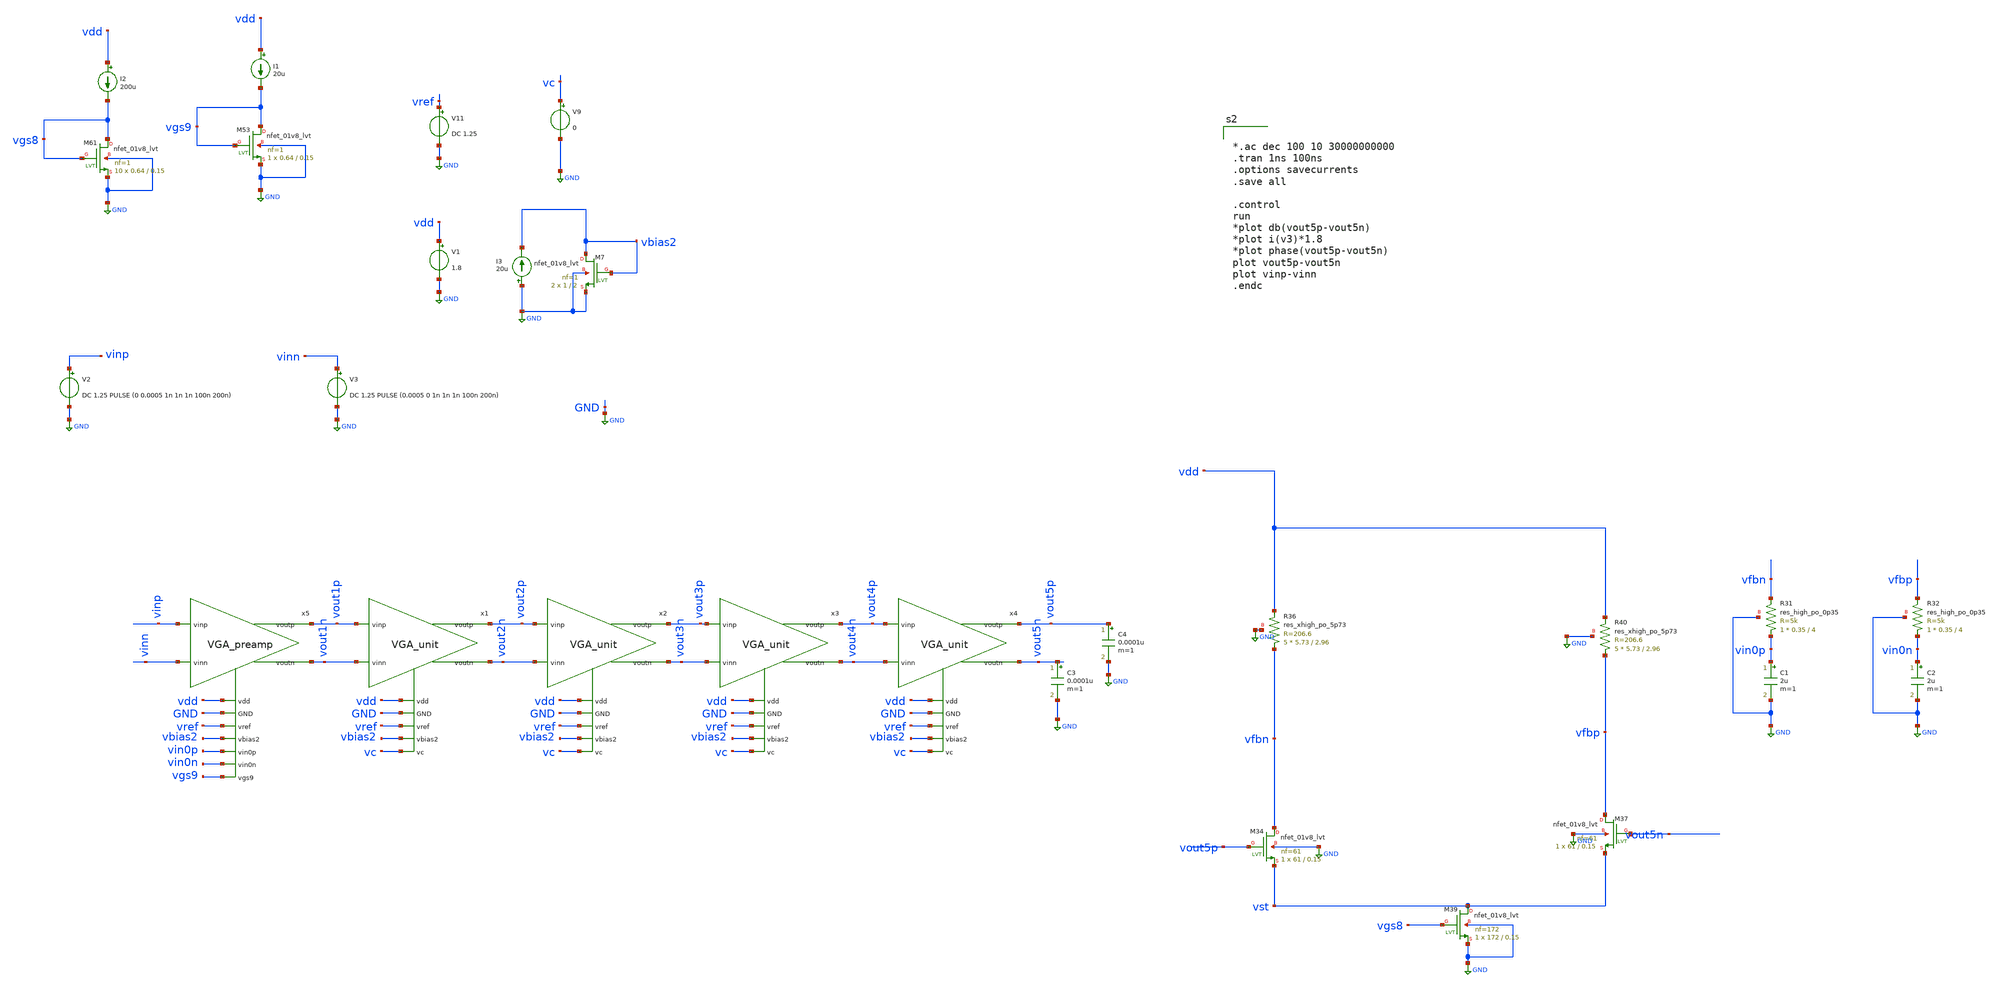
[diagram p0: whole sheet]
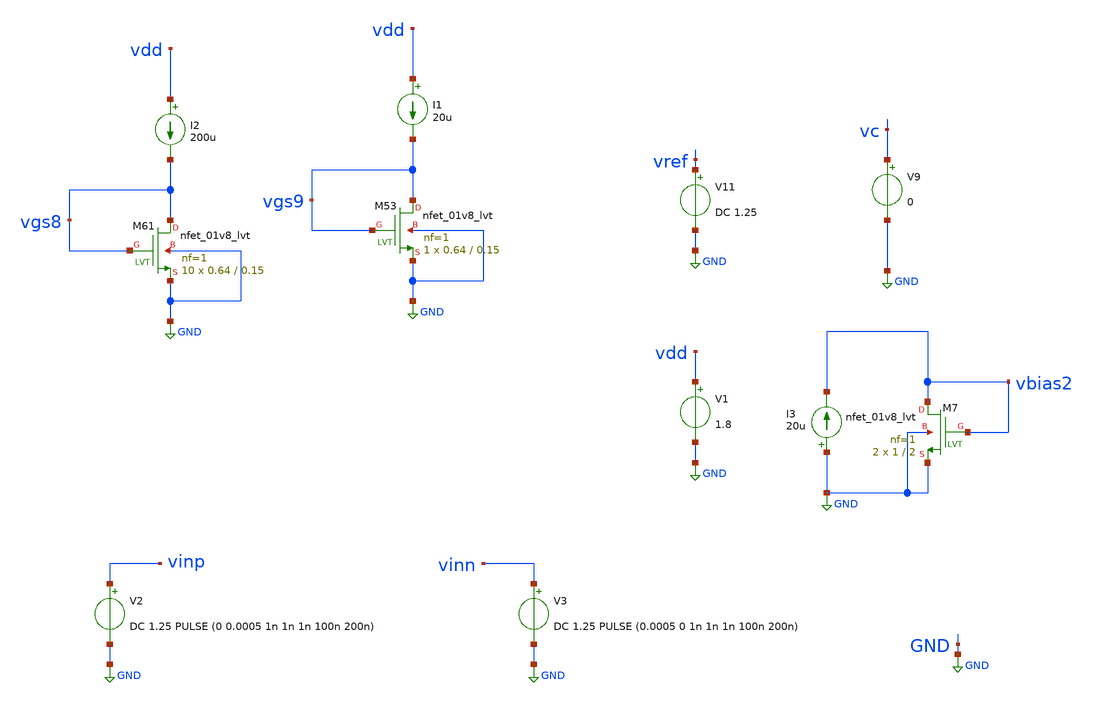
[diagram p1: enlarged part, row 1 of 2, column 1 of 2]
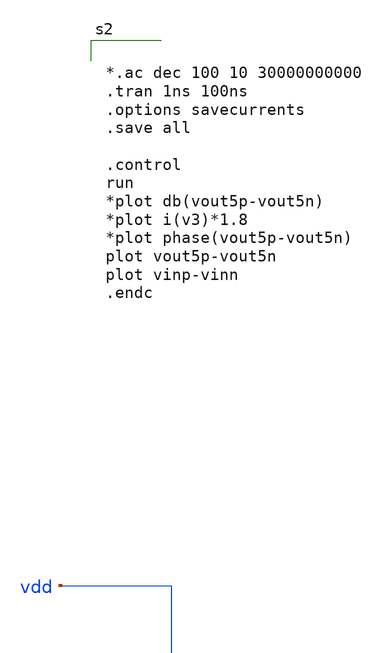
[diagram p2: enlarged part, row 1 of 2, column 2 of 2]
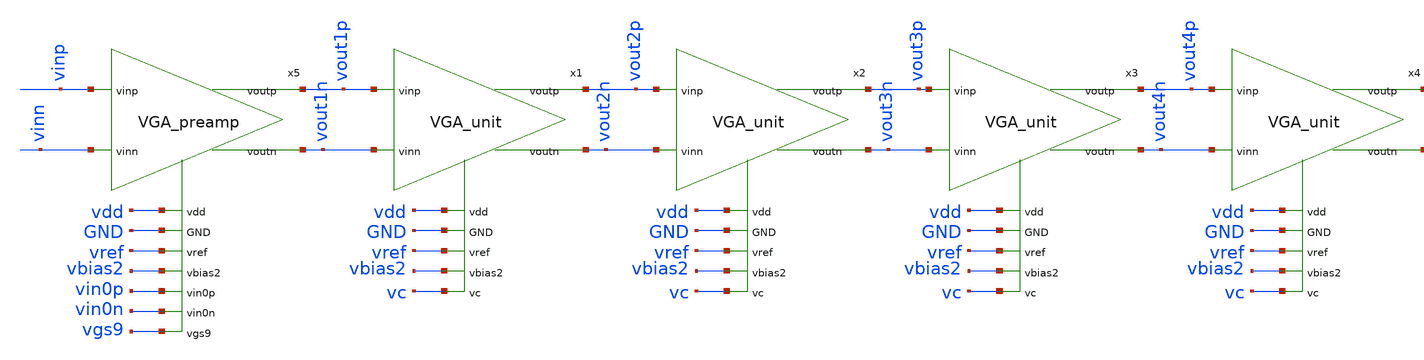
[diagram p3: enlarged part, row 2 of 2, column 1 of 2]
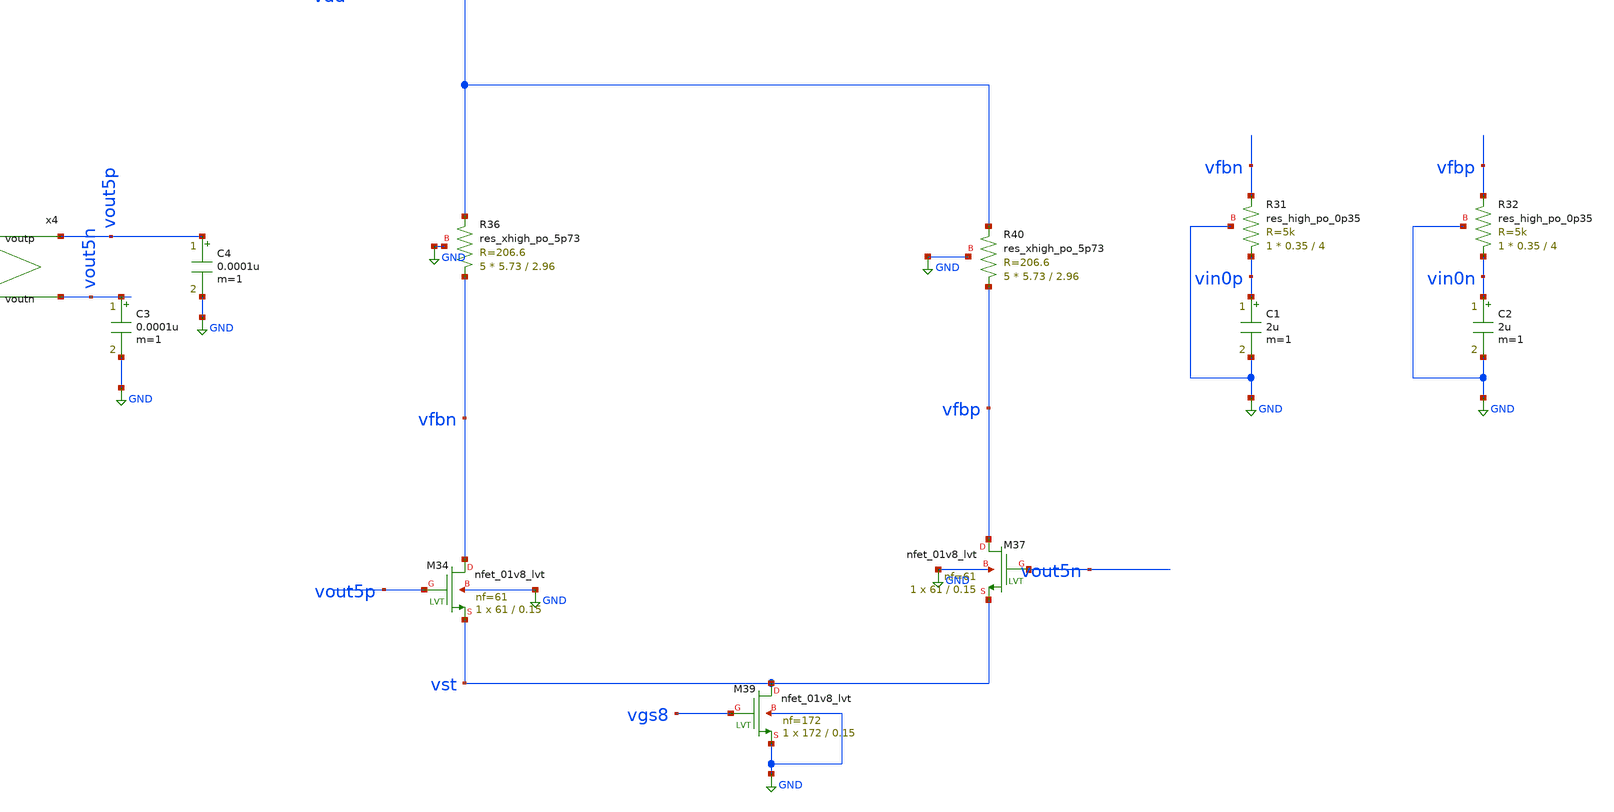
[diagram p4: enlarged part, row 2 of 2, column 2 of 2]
** sch_path: xschem/vga/vga_stability.sch
**.subckt vga_stability
XR36 vfbn vdd GND sky130_fd_pr__res_xhigh_po_5p73 L=2.96 mult=5 m=5
XR40 vfbp vdd GND sky130_fd_pr__res_xhigh_po_5p73 L=2.96 mult=5 m=5
XM34 vfbn vout5p vst GND sky130_fd_pr__nfet_01v8_lvt L=0.15 W=61 nf=61 ad='int((nf+1)/2) * W/nf * 0.29'
+ as='int((nf+2)/2) * W/nf * 0.29' pd='2*int((nf+1)/2) * (W/nf + 0.29)' ps='2*int((nf+2)/2) * (W/nf + 0.29)'
+ nrd='0.29 / W' nrs='0.29 / W' sa=0 sb=0 sd=0 mult=1 m=1
XM37 vfbp vout5n vst GND sky130_fd_pr__nfet_01v8_lvt L=0.15 W=61 nf=61 ad='int((nf+1)/2) * W/nf * 0.29'
+ as='int((nf+2)/2) * W/nf * 0.29' pd='2*int((nf+1)/2) * (W/nf + 0.29)' ps='2*int((nf+2)/2) * (W/nf + 0.29)'
+ nrd='0.29 / W' nrs='0.29 / W' sa=0 sb=0 sd=0 mult=1 m=1
XM39 vst vgs8 GND GND sky130_fd_pr__nfet_01v8_lvt L=0.15 W=172 nf=172 ad='int((nf+1)/2) * W/nf * 0.29'
+ as='int((nf+2)/2) * W/nf * 0.29' pd='2*int((nf+1)/2) * (W/nf + 0.29)' ps='2*int((nf+2)/2) * (W/nf + 0.29)'
+ nrd='0.29 / W' nrs='0.29 / W' sa=0 sb=0 sd=0 mult=1 m=1
C1 vin0p GND 2u m=1
C2 vin0n GND 2u m=1
V9 vc GND 0
V11 vref GND DC 1.25
XM53 vgs9 vgs9 GND GND sky130_fd_pr__nfet_01v8_lvt L=0.15 W=0.64 nf=1 ad='int((nf+1)/2) * W/nf * 0.29'
+ as='int((nf+2)/2) * W/nf * 0.29' pd='2*int((nf+1)/2) * (W/nf + 0.29)' ps='2*int((nf+2)/2) * (W/nf + 0.29)'
+ nrd='0.29 / W' nrs='0.29 / W' sa=0 sb=0 sd=0 mult=1 m=1
I1 vdd vgs9 20u
XR31 vin0p vfbn GND sky130_fd_pr__res_high_po_0p35 L=4 mult=1 m=1
XR32 vin0n vfbp GND sky130_fd_pr__res_high_po_0p35 L=4 mult=1 m=1
XM61 vgs8 vgs8 GND GND sky130_fd_pr__nfet_01v8_lvt L=0.15 W=0.64 nf=1 ad='int((nf+1)/2) * W/nf * 0.29'
+ as='int((nf+2)/2) * W/nf * 0.29' pd='2*int((nf+1)/2) * (W/nf + 0.29)' ps='2*int((nf+2)/2) * (W/nf + 0.29)'
+ nrd='0.29 / W' nrs='0.29 / W' sa=0 sb=0 sd=0 mult=10 m=10
I2 vdd vgs8 200u
x1 vout1p vdd vc vout1n GND vref vout2p vbias2 vout2n VGA_unit
x2 vout2p vdd vc vout2n GND vref vout3p vbias2 vout3n VGA_unit
x3 vout3p vdd vc vout3n GND vref vout4p vbias2 vout4n VGA_unit
x4 vout4p vdd vc vout4n GND vref vout5p vbias2 vout5n VGA_unit
V1 vdd GND 1.8
XM7 vbias2 vbias2 GND GND sky130_fd_pr__nfet_01v8_lvt L=2 W=1 nf=1 ad='int((nf+1)/2) * W/nf * 0.29' as='int((nf+2)/2) * W/nf * 0.29'
+ pd='2*int((nf+1)/2) * (W/nf + 0.29)' ps='2*int((nf+2)/2) * (W/nf + 0.29)' nrd='0.29 / W' nrs='0.29 / W'
+ sa=0 sb=0 sd=0 mult=2 m=2
I3 GND vbias2 20u
V2 vinp GND DC 1.25 PULSE (0 0.0005 1n 1n 1n 100n 200n)
V3 vinn GND DC 1.25 PULSE (0.0005 0 1n 1n 1n 100n 200n)
x5 vdd vinp GND vinn vref vin0p vout1p vin0n vbias2 vout1n vgs9 VGA_preamp
C3 vout5n GND 0.0001u m=1
C4 vout5p GND 0.0001u m=1
**** begin user architecture code

** opencircuitdesign pdks install
.lib $::SKYWATER_MODELS/sky130.lib.spice tt




*.ac dec 100 10 30000000000
.tran 1ns 100ns
.options savecurrents
.save all

.control
run
*plot db(vout5p-vout5n)
*plot i(v3)*1.8
*plot phase(vout5p-vout5n)
plot vout5p-vout5n
plot vinp-vinn
.endc


**** end user architecture code
**.ends

* expanding   symbol:  simulations/VGA_unit.sym # of pins=9
** sym_path: xschem/vga/VGA_unit.sym
** sch_path: xschem/vga/VGA_unit.sch
.subckt VGA_unit vinp vdd vc vinn GND vref voutp vbias2 voutn
*.ipin vinp
*.ipin vinn
*.opin voutp
*.opin voutn
*.ipin vdd
*.ipin GND
*.ipin vref
*.ipin vbias2
*.ipin vc
XR7 vd21 vdd GND sky130_fd_pr__res_xhigh_po_5p73 L=2.96 mult=5 m=5
XR8 voutp vdd GND sky130_fd_pr__res_xhigh_po_5p73 L=2.96 mult=3 m=3
XR9 vd21 voutp GND sky130_fd_pr__res_xhigh_po_5p73 L=7.5 mult=2 m=2
XR10 voutn vdd GND sky130_fd_pr__res_xhigh_po_5p73 L=2.96 mult=3 m=3
XR11 vd22 vdd GND sky130_fd_pr__res_xhigh_po_5p73 L=2.96 mult=5 m=5
XR12 voutn vd22 GND sky130_fd_pr__res_xhigh_po_5p73 L=7.5 mult=2 m=2
XM7 vd21 vinp vs21 GND sky130_fd_pr__nfet_01v8_lvt L=0.15 W=61 nf=61 ad='int((nf+1)/2) * W/nf * 0.29'
+ as='int((nf+2)/2) * W/nf * 0.29' pd='2*int((nf+1)/2) * (W/nf + 0.29)' ps='2*int((nf+2)/2) * (W/nf + 0.29)'
+ nrd='0.29 / W' nrs='0.29 / W' sa=0 sb=0 sd=0 mult=1 m=1
XM8 voutp vd21 vs22 GND sky130_fd_pr__nfet_01v8_lvt L=0.15 W=61 nf=61 ad='int((nf+1)/2) * W/nf * 0.29'
+ as='int((nf+2)/2) * W/nf * 0.29' pd='2*int((nf+1)/2) * (W/nf + 0.29)' ps='2*int((nf+2)/2) * (W/nf + 0.29)'
+ nrd='0.29 / W' nrs='0.29 / W' sa=0 sb=0 sd=0 mult=1 m=1
XM10 voutn vd22 vs22 GND sky130_fd_pr__nfet_01v8_lvt L=0.15 W=61 nf=61 ad='int((nf+1)/2) * W/nf * 0.29'
+ as='int((nf+2)/2) * W/nf * 0.29' pd='2*int((nf+1)/2) * (W/nf + 0.29)' ps='2*int((nf+2)/2) * (W/nf + 0.29)'
+ nrd='0.29 / W' nrs='0.29 / W' sa=0 sb=0 sd=0 mult=1 m=1
XM11 vd22 vinn vs21 GND sky130_fd_pr__nfet_01v8_lvt L=0.15 W=61 nf=61 ad='int((nf+1)/2) * W/nf * 0.29'
+ as='int((nf+2)/2) * W/nf * 0.29' pd='2*int((nf+1)/2) * (W/nf + 0.29)' ps='2*int((nf+2)/2) * (W/nf + 0.29)'
+ nrd='0.29 / W' nrs='0.29 / W' sa=0 sb=0 sd=0 mult=1 m=1
XM12 vs22 vo22 GND GND sky130_fd_pr__nfet_01v8_lvt L=0.15 W=172 nf=172 ad='int((nf+1)/2) * W/nf * 0.29'
+ as='int((nf+2)/2) * W/nf * 0.29' pd='2*int((nf+1)/2) * (W/nf + 0.29)' ps='2*int((nf+2)/2) * (W/nf + 0.29)'
+ nrd='0.29 / W' nrs='0.29 / W' sa=0 sb=0 sd=0 mult=1 m=1
XM13 vs21 vo21 GND GND sky130_fd_pr__nfet_01v8_lvt L=0.15 W=172 nf=172 ad='int((nf+1)/2) * W/nf * 0.29'
+ as='int((nf+2)/2) * W/nf * 0.29' pd='2*int((nf+1)/2) * (W/nf + 0.29)' ps='2*int((nf+2)/2) * (W/nf + 0.29)'
+ nrd='0.29 / W' nrs='0.29 / W' sa=0 sb=0 sd=0 mult=1 m=1
XM32 vd21 vc voutp GND sky130_fd_pr__nfet_01v8_lvt L=0.15 W=1 nf=1 ad='int((nf+1)/2) * W/nf * 0.29' as='int((nf+2)/2) * W/nf * 0.29'
+ pd='2*int((nf+1)/2) * (W/nf + 0.29)' ps='2*int((nf+2)/2) * (W/nf + 0.29)' nrd='0.29 / W' nrs='0.29 / W'
+ sa=0 sb=0 sd=0 mult=1 m=1
XM33 voutn vc vd22 GND sky130_fd_pr__nfet_01v8_lvt L=0.15 W=1 nf=1 ad='int((nf+1)/2) * W/nf * 0.29' as='int((nf+2)/2) * W/nf * 0.29'
+ pd='2*int((nf+1)/2) * (W/nf + 0.29)' ps='2*int((nf+2)/2) * (W/nf + 0.29)' nrd='0.29 / W' nrs='0.29 / W'
+ sa=0 sb=0 sd=0 mult=1 m=1
XM62 net2 vref net1 GND sky130_fd_pr__nfet_01v8_lvt L=0.25 W=1 nf=1 ad='int((nf+1)/2) * W/nf * 0.29'
+ as='int((nf+2)/2) * W/nf * 0.29' pd='2*int((nf+1)/2) * (W/nf + 0.29)' ps='2*int((nf+2)/2) * (W/nf + 0.29)'
+ nrd='0.29 / W' nrs='0.29 / W' sa=0 sb=0 sd=0 mult=1 m=1
XM63 net3 vcm21 net1 GND sky130_fd_pr__nfet_01v8_lvt L=0.25 W=1 nf=1 ad='int((nf+1)/2) * W/nf * 0.29'
+ as='int((nf+2)/2) * W/nf * 0.29' pd='2*int((nf+1)/2) * (W/nf + 0.29)' ps='2*int((nf+2)/2) * (W/nf + 0.29)'
+ nrd='0.29 / W' nrs='0.29 / W' sa=0 sb=0 sd=0 mult=1 m=1
XM64 net1 vbias2 GND GND sky130_fd_pr__nfet_01v8_lvt L=2 W=1 nf=1 ad='int((nf+1)/2) * W/nf * 0.29' as='int((nf+2)/2) * W/nf * 0.29'
+ pd='2*int((nf+1)/2) * (W/nf + 0.29)' ps='2*int((nf+2)/2) * (W/nf + 0.29)' nrd='0.29 / W' nrs='0.29 / W'
+ sa=0 sb=0 sd=0 mult=2 m=2
XM65 vo21 vbias2 GND GND sky130_fd_pr__nfet_01v8_lvt L=2 W=1 nf=1 ad='int((nf+1)/2) * W/nf * 0.29' as='int((nf+2)/2) * W/nf * 0.29'
+ pd='2*int((nf+1)/2) * (W/nf + 0.29)' ps='2*int((nf+2)/2) * (W/nf + 0.29)' nrd='0.29 / W' nrs='0.29 / W'
+ sa=0 sb=0 sd=0 mult=10 m=10
XM66 net3 net2 vdd vdd sky130_fd_pr__pfet_01v8_lvt L=0.5 W=1 nf=1 ad='int((nf+1)/2) * W/nf * 0.29' as='int((nf+2)/2) * W/nf * 0.29'
+ pd='2*int((nf+1)/2) * (W/nf + 0.29)' ps='2*int((nf+2)/2) * (W/nf + 0.29)' nrd='0.29 / W' nrs='0.29 / W'
+ sa=0 sb=0 sd=0 mult=1 m=1
XM67 net2 net2 vdd vdd sky130_fd_pr__pfet_01v8_lvt L=0.5 W=1 nf=1 ad='int((nf+1)/2) * W/nf * 0.29' as='int((nf+2)/2) * W/nf * 0.29'
+ pd='2*int((nf+1)/2) * (W/nf + 0.29)' ps='2*int((nf+2)/2) * (W/nf + 0.29)' nrd='0.29 / W' nrs='0.29 / W'
+ sa=0 sb=0 sd=0 mult=1 m=1
XM68 vo21 net3 vdd vdd sky130_fd_pr__pfet_01v8_lvt L=0.5 W=1 nf=1 ad='int((nf+1)/2) * W/nf * 0.29' as='int((nf+2)/2) * W/nf * 0.29'
+ pd='2*int((nf+1)/2) * (W/nf + 0.29)' ps='2*int((nf+2)/2) * (W/nf + 0.29)' nrd='0.29 / W' nrs='0.29 / W'
+ sa=0 sb=0 sd=0 mult=10 m=10
XC5 net7 vo21 sky130_fd_pr__cap_mim_m3_1 W=50 L=50 MF=1 m=1
XM70 net5 vref net4 GND sky130_fd_pr__nfet_01v8_lvt L=0.25 W=1 nf=1 ad='int((nf+1)/2) * W/nf * 0.29'
+ as='int((nf+2)/2) * W/nf * 0.29' pd='2*int((nf+1)/2) * (W/nf + 0.29)' ps='2*int((nf+2)/2) * (W/nf + 0.29)'
+ nrd='0.29 / W' nrs='0.29 / W' sa=0 sb=0 sd=0 mult=1 m=1
XM71 net6 vcm22 net4 GND sky130_fd_pr__nfet_01v8_lvt L=0.25 W=1 nf=1 ad='int((nf+1)/2) * W/nf * 0.29'
+ as='int((nf+2)/2) * W/nf * 0.29' pd='2*int((nf+1)/2) * (W/nf + 0.29)' ps='2*int((nf+2)/2) * (W/nf + 0.29)'
+ nrd='0.29 / W' nrs='0.29 / W' sa=0 sb=0 sd=0 mult=1 m=1
XM72 net4 vbias2 GND GND sky130_fd_pr__nfet_01v8_lvt L=2 W=1 nf=1 ad='int((nf+1)/2) * W/nf * 0.29' as='int((nf+2)/2) * W/nf * 0.29'
+ pd='2*int((nf+1)/2) * (W/nf + 0.29)' ps='2*int((nf+2)/2) * (W/nf + 0.29)' nrd='0.29 / W' nrs='0.29 / W'
+ sa=0 sb=0 sd=0 mult=2 m=2
XM73 vo22 vbias2 GND GND sky130_fd_pr__nfet_01v8_lvt L=2 W=1 nf=1 ad='int((nf+1)/2) * W/nf * 0.29' as='int((nf+2)/2) * W/nf * 0.29'
+ pd='2*int((nf+1)/2) * (W/nf + 0.29)' ps='2*int((nf+2)/2) * (W/nf + 0.29)' nrd='0.29 / W' nrs='0.29 / W'
+ sa=0 sb=0 sd=0 mult=10 m=10
XM74 net6 net5 vdd vdd sky130_fd_pr__pfet_01v8_lvt L=0.5 W=1 nf=1 ad='int((nf+1)/2) * W/nf * 0.29' as='int((nf+2)/2) * W/nf * 0.29'
+ pd='2*int((nf+1)/2) * (W/nf + 0.29)' ps='2*int((nf+2)/2) * (W/nf + 0.29)' nrd='0.29 / W' nrs='0.29 / W'
+ sa=0 sb=0 sd=0 mult=1 m=1
XM75 net5 net5 vdd vdd sky130_fd_pr__pfet_01v8_lvt L=0.5 W=1 nf=1 ad='int((nf+1)/2) * W/nf * 0.29' as='int((nf+2)/2) * W/nf * 0.29'
+ pd='2*int((nf+1)/2) * (W/nf + 0.29)' ps='2*int((nf+2)/2) * (W/nf + 0.29)' nrd='0.29 / W' nrs='0.29 / W'
+ sa=0 sb=0 sd=0 mult=1 m=1
XM76 vo22 net6 vdd vdd sky130_fd_pr__pfet_01v8_lvt L=0.5 W=1 nf=1 ad='int((nf+1)/2) * W/nf * 0.29' as='int((nf+2)/2) * W/nf * 0.29'
+ pd='2*int((nf+1)/2) * (W/nf + 0.29)' ps='2*int((nf+2)/2) * (W/nf + 0.29)' nrd='0.29 / W' nrs='0.29 / W'
+ sa=0 sb=0 sd=0 mult=10 m=10
XC6 net8 vo22 sky130_fd_pr__cap_mim_m3_1 W=50 L=50 MF=1 m=1
XR43 vd21 vcm21 GND sky130_fd_pr__res_xhigh_po_5p73 L=5.92 mult=1 m=1
XR44 vcm21 vd22 GND sky130_fd_pr__res_xhigh_po_5p73 L=5.92 mult=1 m=1
XR45 voutp vcm22 GND sky130_fd_pr__res_xhigh_po_5p73 L=5.92 mult=1 m=1
XR46 vcm22 voutn GND sky130_fd_pr__res_xhigh_po_5p73 L=5.92 mult=1 m=1
XR41 net7 net3 GND sky130_fd_pr__res_high_po_0p35 L=4 mult=1 m=1
XR42 net8 net6 GND sky130_fd_pr__res_high_po_0p35 L=4 mult=1 m=1
.ends


* expanding   symbol:  simulations/VGA_preamp.sym # of pins=11
** sym_path: xschem/vga/VGA_preamp.sym
** sch_path: xschem/vga/VGA_preamp.sch
.subckt VGA_preamp vdd vinp GND vinn vref vin0p voutp vin0n vbias2 voutn vgs9
*.ipin vinp
*.ipin vinn
*.opin voutp
*.opin voutn
*.ipin vdd
*.ipin GND
*.ipin vref
*.ipin vbias2
*.ipin vin0p
*.ipin vin0n
*.ipin vgs9
XR1 vd11 vdd GND sky130_fd_pr__res_xhigh_po_5p73 L=2.96 mult=5 m=5
XR2 voutp vdd GND sky130_fd_pr__res_xhigh_po_5p73 L=2.96 mult=3 m=3
XR3 vd11 voutp GND sky130_fd_pr__res_xhigh_po_5p73 L=7.5 mult=2 m=2
XR4 voutn vdd GND sky130_fd_pr__res_xhigh_po_5p73 L=2.96 mult=3 m=3
XR5 vd12 vdd GND sky130_fd_pr__res_xhigh_po_5p73 L=2.96 mult=5 m=5
XR6 voutn vd12 GND sky130_fd_pr__res_xhigh_po_5p73 L=7.5 mult=2 m=2
XM1 vd11 vinp vs11 GND sky130_fd_pr__nfet_01v8_lvt L=0.15 W=61 nf=61 ad='int((nf+1)/2) * W/nf * 0.29'
+ as='int((nf+2)/2) * W/nf * 0.29' pd='2*int((nf+1)/2) * (W/nf + 0.29)' ps='2*int((nf+2)/2) * (W/nf + 0.29)'
+ nrd='0.29 / W' nrs='0.29 / W' sa=0 sb=0 sd=0 mult=1 m=1
XM2 voutp vd11 vs12 GND sky130_fd_pr__nfet_01v8_lvt L=0.15 W=61 nf=61 ad='int((nf+1)/2) * W/nf * 0.29'
+ as='int((nf+2)/2) * W/nf * 0.29' pd='2*int((nf+1)/2) * (W/nf + 0.29)' ps='2*int((nf+2)/2) * (W/nf + 0.29)'
+ nrd='0.29 / W' nrs='0.29 / W' sa=0 sb=0 sd=0 mult=1 m=1
XM3 voutn vd12 vs12 GND sky130_fd_pr__nfet_01v8_lvt L=0.15 W=61 nf=61 ad='int((nf+1)/2) * W/nf * 0.29'
+ as='int((nf+2)/2) * W/nf * 0.29' pd='2*int((nf+1)/2) * (W/nf + 0.29)' ps='2*int((nf+2)/2) * (W/nf + 0.29)'
+ nrd='0.29 / W' nrs='0.29 / W' sa=0 sb=0 sd=0 mult=1 m=1
XM4 vd12 vinn vs11 GND sky130_fd_pr__nfet_01v8_lvt L=0.15 W=61 nf=61 ad='int((nf+1)/2) * W/nf * 0.29'
+ as='int((nf+2)/2) * W/nf * 0.29' pd='2*int((nf+1)/2) * (W/nf + 0.29)' ps='2*int((nf+2)/2) * (W/nf + 0.29)'
+ nrd='0.29 / W' nrs='0.29 / W' sa=0 sb=0 sd=0 mult=1 m=1
XM5 vs12 vo2 GND GND sky130_fd_pr__nfet_01v8_lvt L=0.15 W=172 nf=172 ad='int((nf+1)/2) * W/nf * 0.29'
+ as='int((nf+2)/2) * W/nf * 0.29' pd='2*int((nf+1)/2) * (W/nf + 0.29)' ps='2*int((nf+2)/2) * (W/nf + 0.29)'
+ nrd='0.29 / W' nrs='0.29 / W' sa=0 sb=0 sd=0 mult=1 m=1
XM6 vs11 vo GND GND sky130_fd_pr__nfet_01v8_lvt L=0.15 W=172 nf=172 ad='int((nf+1)/2) * W/nf * 0.29'
+ as='int((nf+2)/2) * W/nf * 0.29' pd='2*int((nf+1)/2) * (W/nf + 0.29)' ps='2*int((nf+2)/2) * (W/nf + 0.29)'
+ nrd='0.29 / W' nrs='0.29 / W' sa=0 sb=0 sd=0 mult=1 m=1
XM46 net2 vref net1 GND sky130_fd_pr__nfet_01v8_lvt L=0.25 W=1 nf=1 ad='int((nf+1)/2) * W/nf * 0.29'
+ as='int((nf+2)/2) * W/nf * 0.29' pd='2*int((nf+1)/2) * (W/nf + 0.29)' ps='2*int((nf+2)/2) * (W/nf + 0.29)'
+ nrd='0.29 / W' nrs='0.29 / W' sa=0 sb=0 sd=0 mult=1 m=1
XM47 net3 vcm net1 GND sky130_fd_pr__nfet_01v8_lvt L=0.25 W=1 nf=1 ad='int((nf+1)/2) * W/nf * 0.29' as='int((nf+2)/2) * W/nf * 0.29'
+ pd='2*int((nf+1)/2) * (W/nf + 0.29)' ps='2*int((nf+2)/2) * (W/nf + 0.29)' nrd='0.29 / W' nrs='0.29 / W'
+ sa=0 sb=0 sd=0 mult=1 m=1
XM48 net1 vbias2 GND GND sky130_fd_pr__nfet_01v8_lvt L=2 W=1 nf=1 ad='int((nf+1)/2) * W/nf * 0.29' as='int((nf+2)/2) * W/nf * 0.29'
+ pd='2*int((nf+1)/2) * (W/nf + 0.29)' ps='2*int((nf+2)/2) * (W/nf + 0.29)' nrd='0.29 / W' nrs='0.29 / W'
+ sa=0 sb=0 sd=0 mult=2 m=2
XM49 vo vbias2 GND GND sky130_fd_pr__nfet_01v8_lvt L=2 W=1 nf=1 ad='int((nf+1)/2) * W/nf * 0.29' as='int((nf+2)/2) * W/nf * 0.29'
+ pd='2*int((nf+1)/2) * (W/nf + 0.29)' ps='2*int((nf+2)/2) * (W/nf + 0.29)' nrd='0.29 / W' nrs='0.29 / W'
+ sa=0 sb=0 sd=0 mult=10 m=10
XM50 net3 net2 vdd vdd sky130_fd_pr__pfet_01v8_lvt L=0.5 W=1 nf=1 ad='int((nf+1)/2) * W/nf * 0.29' as='int((nf+2)/2) * W/nf * 0.29'
+ pd='2*int((nf+1)/2) * (W/nf + 0.29)' ps='2*int((nf+2)/2) * (W/nf + 0.29)' nrd='0.29 / W' nrs='0.29 / W'
+ sa=0 sb=0 sd=0 mult=1 m=1
XM51 net2 net2 vdd vdd sky130_fd_pr__pfet_01v8_lvt L=0.5 W=1 nf=1 ad='int((nf+1)/2) * W/nf * 0.29' as='int((nf+2)/2) * W/nf * 0.29'
+ pd='2*int((nf+1)/2) * (W/nf + 0.29)' ps='2*int((nf+2)/2) * (W/nf + 0.29)' nrd='0.29 / W' nrs='0.29 / W'
+ sa=0 sb=0 sd=0 mult=1 m=1
XM52 vo net3 vdd vdd sky130_fd_pr__pfet_01v8_lvt L=0.5 W=1 nf=1 ad='int((nf+1)/2) * W/nf * 0.29' as='int((nf+2)/2) * W/nf * 0.29'
+ pd='2*int((nf+1)/2) * (W/nf + 0.29)' ps='2*int((nf+2)/2) * (W/nf + 0.29)' nrd='0.29 / W' nrs='0.29 / W'
+ sa=0 sb=0 sd=0 mult=10 m=10
XC3 net7 vo sky130_fd_pr__cap_mim_m3_1 W=50 L=50 MF=1 m=1
XM54 net5 vref net4 GND sky130_fd_pr__nfet_01v8_lvt L=0.25 W=1 nf=1 ad='int((nf+1)/2) * W/nf * 0.29'
+ as='int((nf+2)/2) * W/nf * 0.29' pd='2*int((nf+1)/2) * (W/nf + 0.29)' ps='2*int((nf+2)/2) * (W/nf + 0.29)'
+ nrd='0.29 / W' nrs='0.29 / W' sa=0 sb=0 sd=0 mult=1 m=1
XM55 net6 vcm2 net4 GND sky130_fd_pr__nfet_01v8_lvt L=0.25 W=1 nf=1 ad='int((nf+1)/2) * W/nf * 0.29'
+ as='int((nf+2)/2) * W/nf * 0.29' pd='2*int((nf+1)/2) * (W/nf + 0.29)' ps='2*int((nf+2)/2) * (W/nf + 0.29)'
+ nrd='0.29 / W' nrs='0.29 / W' sa=0 sb=0 sd=0 mult=1 m=1
XM56 net4 vbias2 GND GND sky130_fd_pr__nfet_01v8_lvt L=2 W=1 nf=1 ad='int((nf+1)/2) * W/nf * 0.29' as='int((nf+2)/2) * W/nf * 0.29'
+ pd='2*int((nf+1)/2) * (W/nf + 0.29)' ps='2*int((nf+2)/2) * (W/nf + 0.29)' nrd='0.29 / W' nrs='0.29 / W'
+ sa=0 sb=0 sd=0 mult=2 m=2
XM57 vo2 vbias2 GND GND sky130_fd_pr__nfet_01v8_lvt L=2 W=1 nf=1 ad='int((nf+1)/2) * W/nf * 0.29' as='int((nf+2)/2) * W/nf * 0.29'
+ pd='2*int((nf+1)/2) * (W/nf + 0.29)' ps='2*int((nf+2)/2) * (W/nf + 0.29)' nrd='0.29 / W' nrs='0.29 / W'
+ sa=0 sb=0 sd=0 mult=10 m=10
XM58 net6 net5 vdd vdd sky130_fd_pr__pfet_01v8_lvt L=0.5 W=1 nf=1 ad='int((nf+1)/2) * W/nf * 0.29' as='int((nf+2)/2) * W/nf * 0.29'
+ pd='2*int((nf+1)/2) * (W/nf + 0.29)' ps='2*int((nf+2)/2) * (W/nf + 0.29)' nrd='0.29 / W' nrs='0.29 / W'
+ sa=0 sb=0 sd=0 mult=1 m=1
XM59 net5 net5 vdd vdd sky130_fd_pr__pfet_01v8_lvt L=0.5 W=1 nf=1 ad='int((nf+1)/2) * W/nf * 0.29' as='int((nf+2)/2) * W/nf * 0.29'
+ pd='2*int((nf+1)/2) * (W/nf + 0.29)' ps='2*int((nf+2)/2) * (W/nf + 0.29)' nrd='0.29 / W' nrs='0.29 / W'
+ sa=0 sb=0 sd=0 mult=1 m=1
XM60 vo2 net6 vdd vdd sky130_fd_pr__pfet_01v8_lvt L=0.5 W=1 nf=1 ad='int((nf+1)/2) * W/nf * 0.29' as='int((nf+2)/2) * W/nf * 0.29'
+ pd='2*int((nf+1)/2) * (W/nf + 0.29)' ps='2*int((nf+2)/2) * (W/nf + 0.29)' nrd='0.29 / W' nrs='0.29 / W'
+ sa=0 sb=0 sd=0 mult=10 m=10
XC4 net8 vo2 sky130_fd_pr__cap_mim_m3_1 W=50 L=50 MF=1 m=1
XR33 net7 net3 GND sky130_fd_pr__res_high_po_0p35 L=4 mult=1 m=1
XR34 net8 net6 GND sky130_fd_pr__res_high_po_0p35 L=4 mult=1 m=1
XR35 vd11 vcm GND sky130_fd_pr__res_xhigh_po_5p73 L=5.92 mult=1 m=1
XR37 vcm vd12 GND sky130_fd_pr__res_xhigh_po_5p73 L=5.92 mult=1 m=1
XR38 voutp vcm2 GND sky130_fd_pr__res_xhigh_po_5p73 L=5.92 mult=1 m=1
XR39 vcm2 voutn GND sky130_fd_pr__res_xhigh_po_5p73 L=5.92 mult=1 m=1
XM41 vd11 vin0p net9 GND sky130_fd_pr__nfet_01v8_lvt L=0.15 W=1 nf=1 ad='int((nf+1)/2) * W/nf * 0.29'
+ as='int((nf+2)/2) * W/nf * 0.29' pd='2*int((nf+1)/2) * (W/nf + 0.29)' ps='2*int((nf+2)/2) * (W/nf + 0.29)'
+ nrd='0.29 / W' nrs='0.29 / W' sa=0 sb=0 sd=0 mult=10 m=10
XM42 vd12 vin0n net9 GND sky130_fd_pr__nfet_01v8_lvt L=0.15 W=1 nf=1 ad='int((nf+1)/2) * W/nf * 0.29'
+ as='int((nf+2)/2) * W/nf * 0.29' pd='2*int((nf+1)/2) * (W/nf + 0.29)' ps='2*int((nf+2)/2) * (W/nf + 0.29)'
+ nrd='0.29 / W' nrs='0.29 / W' sa=0 sb=0 sd=0 mult=10 m=10
XM43 net9 vgs9 GND GND sky130_fd_pr__nfet_01v8_lvt L=0.15 W=1 nf=1 ad='int((nf+1)/2) * W/nf * 0.29' as='int((nf+2)/2) * W/nf * 0.29'
+ pd='2*int((nf+1)/2) * (W/nf + 0.29)' ps='2*int((nf+2)/2) * (W/nf + 0.29)' nrd='0.29 / W' nrs='0.29 / W'
+ sa=0 sb=0 sd=0 mult=28 m=28
.ends

.GLOBAL GND
.end
